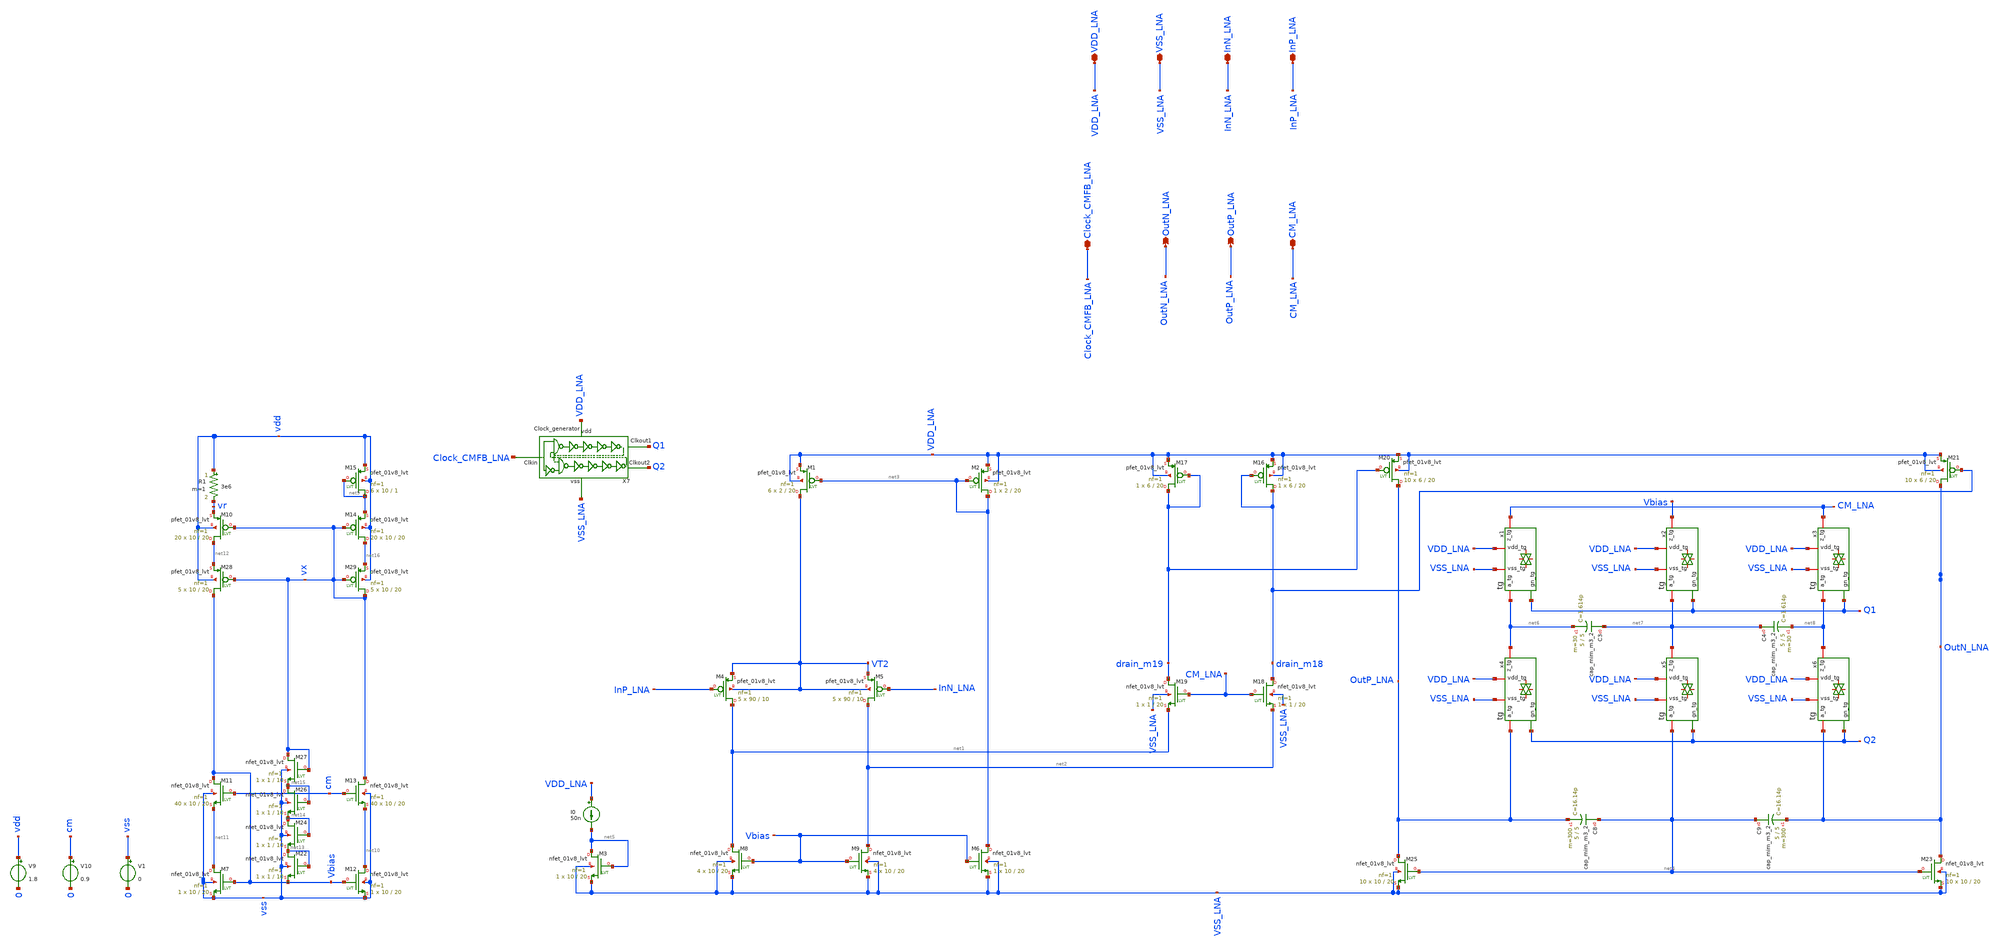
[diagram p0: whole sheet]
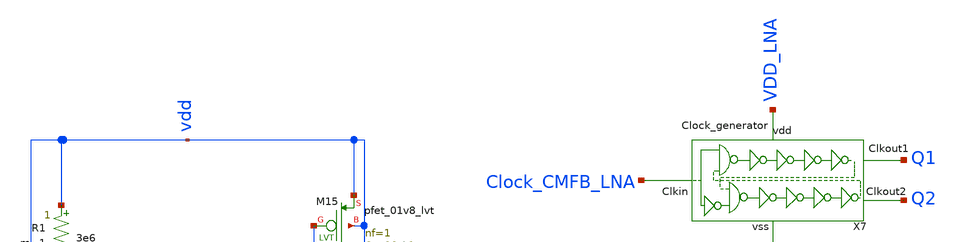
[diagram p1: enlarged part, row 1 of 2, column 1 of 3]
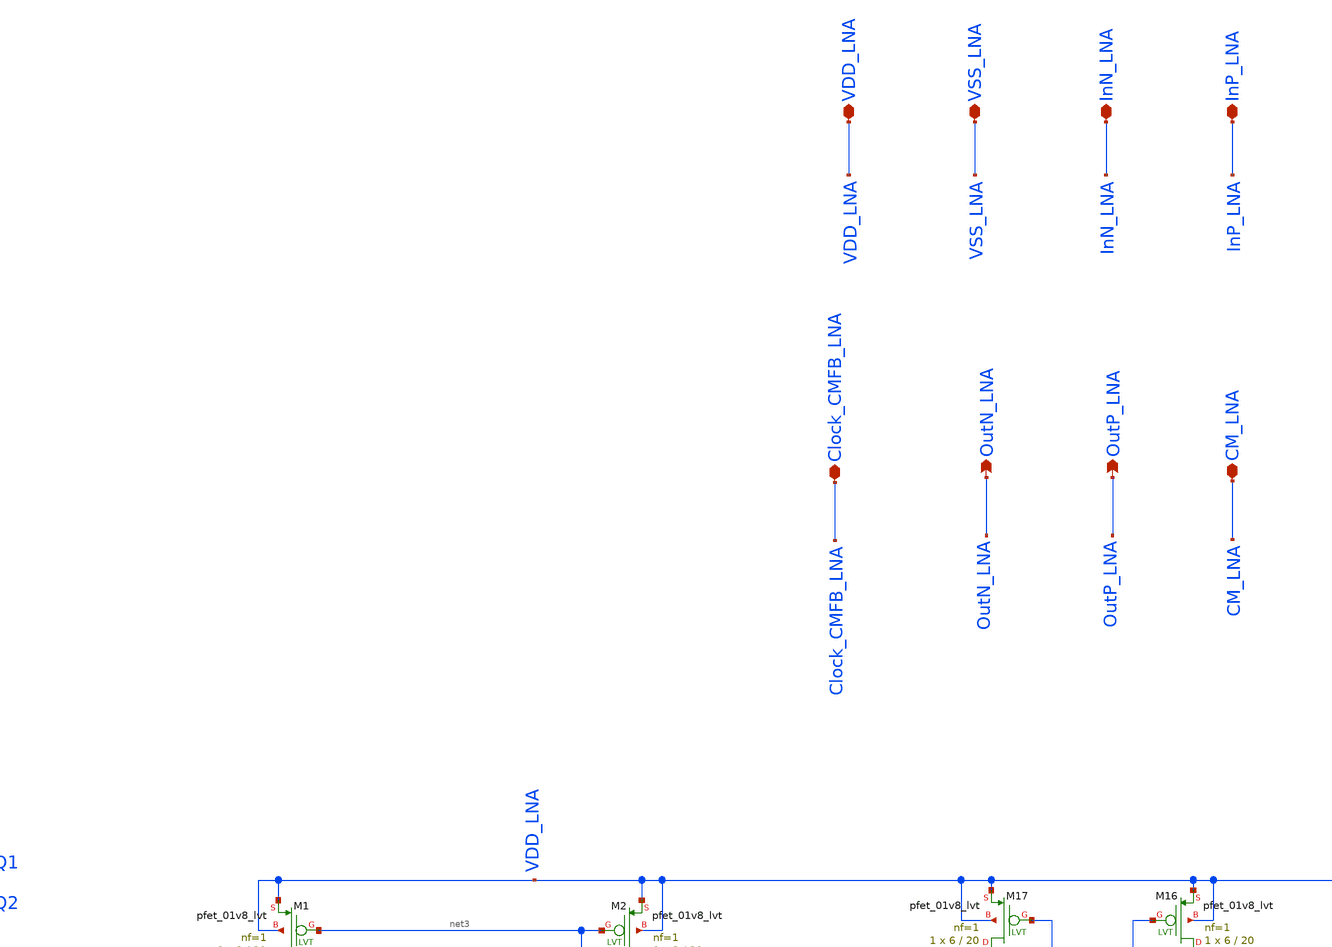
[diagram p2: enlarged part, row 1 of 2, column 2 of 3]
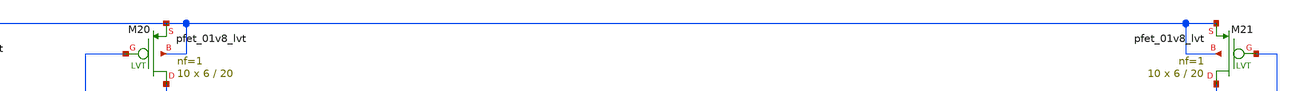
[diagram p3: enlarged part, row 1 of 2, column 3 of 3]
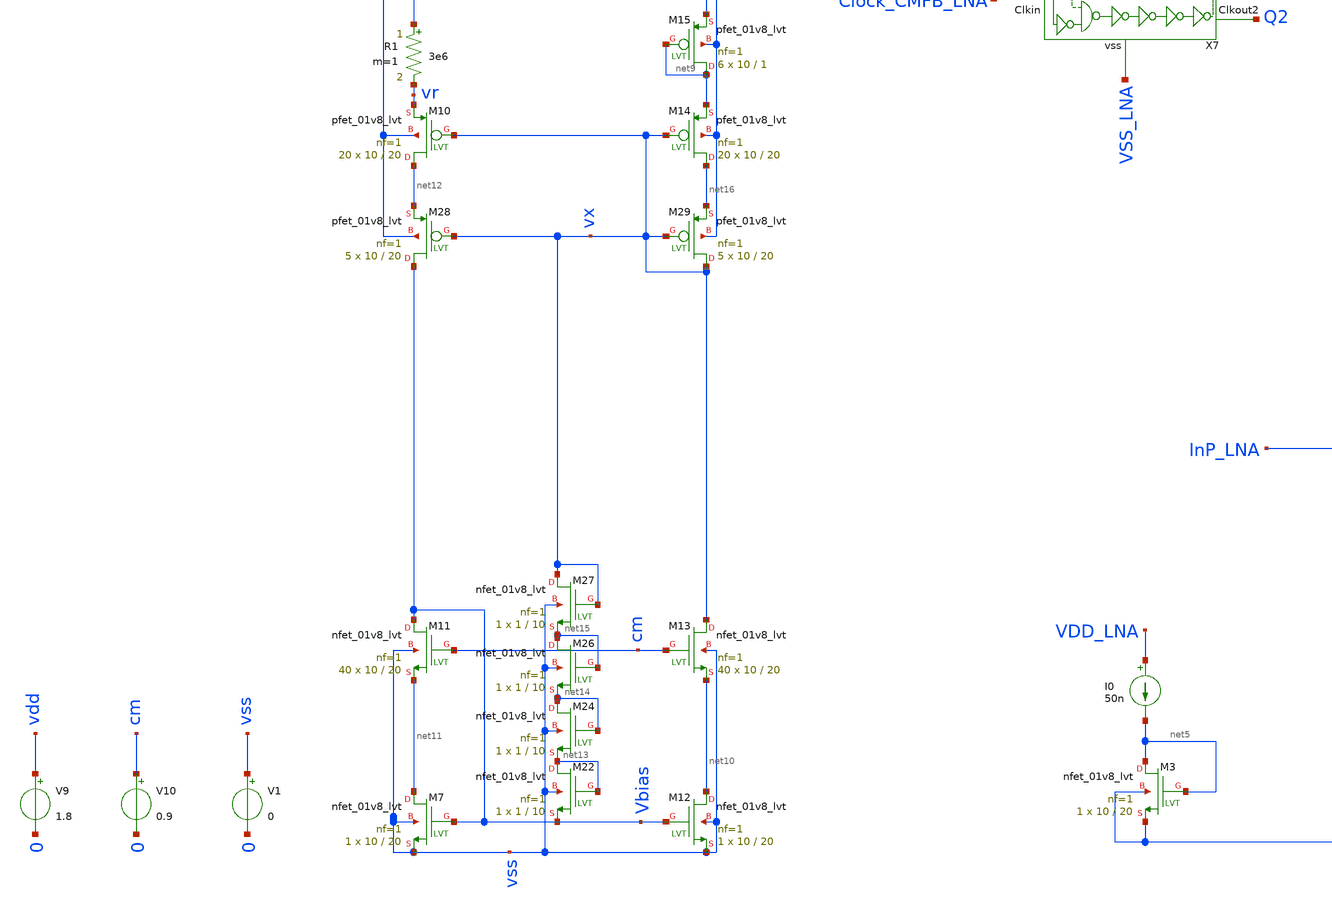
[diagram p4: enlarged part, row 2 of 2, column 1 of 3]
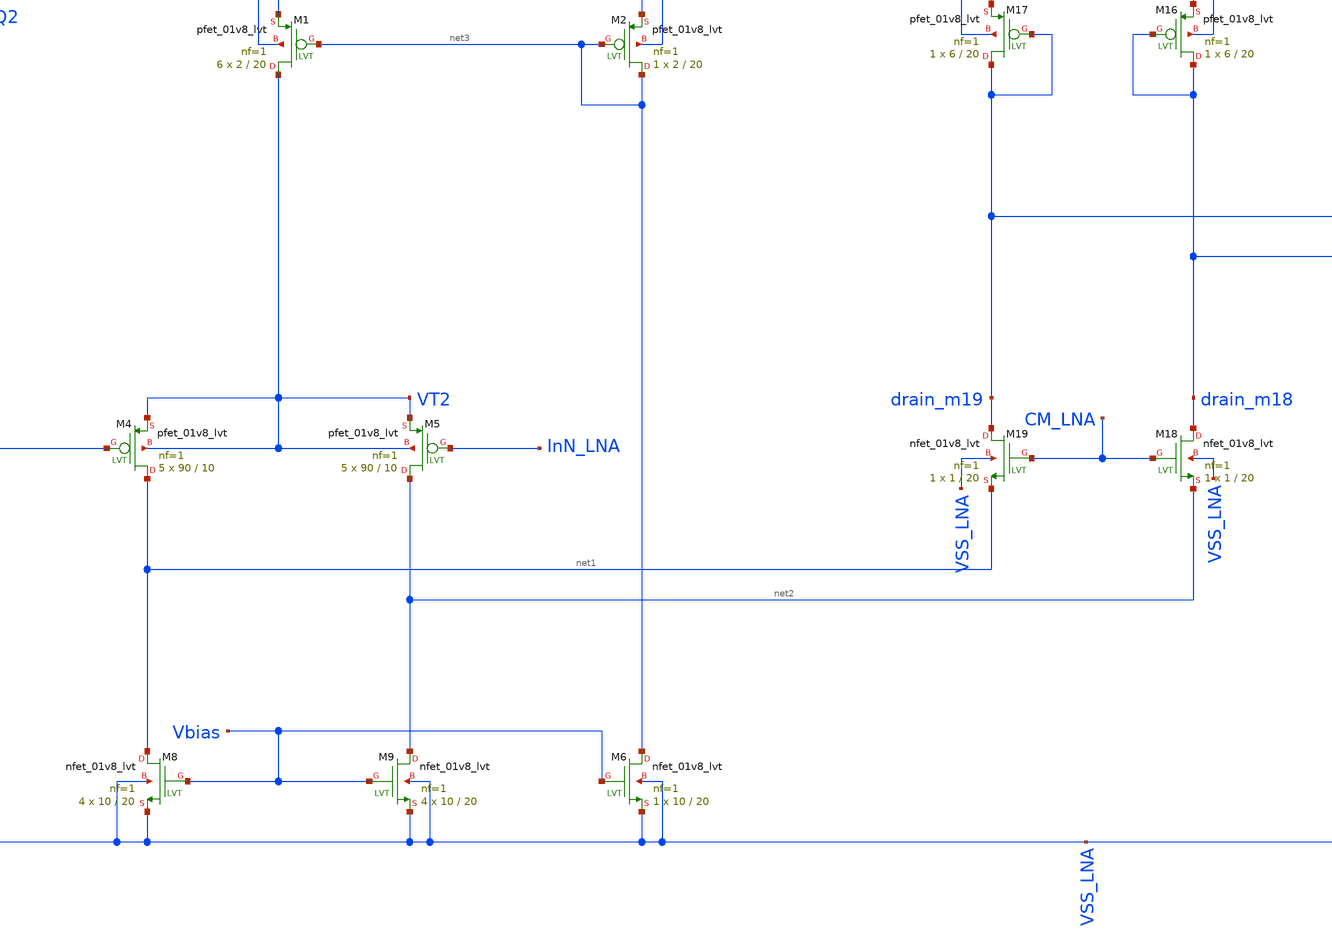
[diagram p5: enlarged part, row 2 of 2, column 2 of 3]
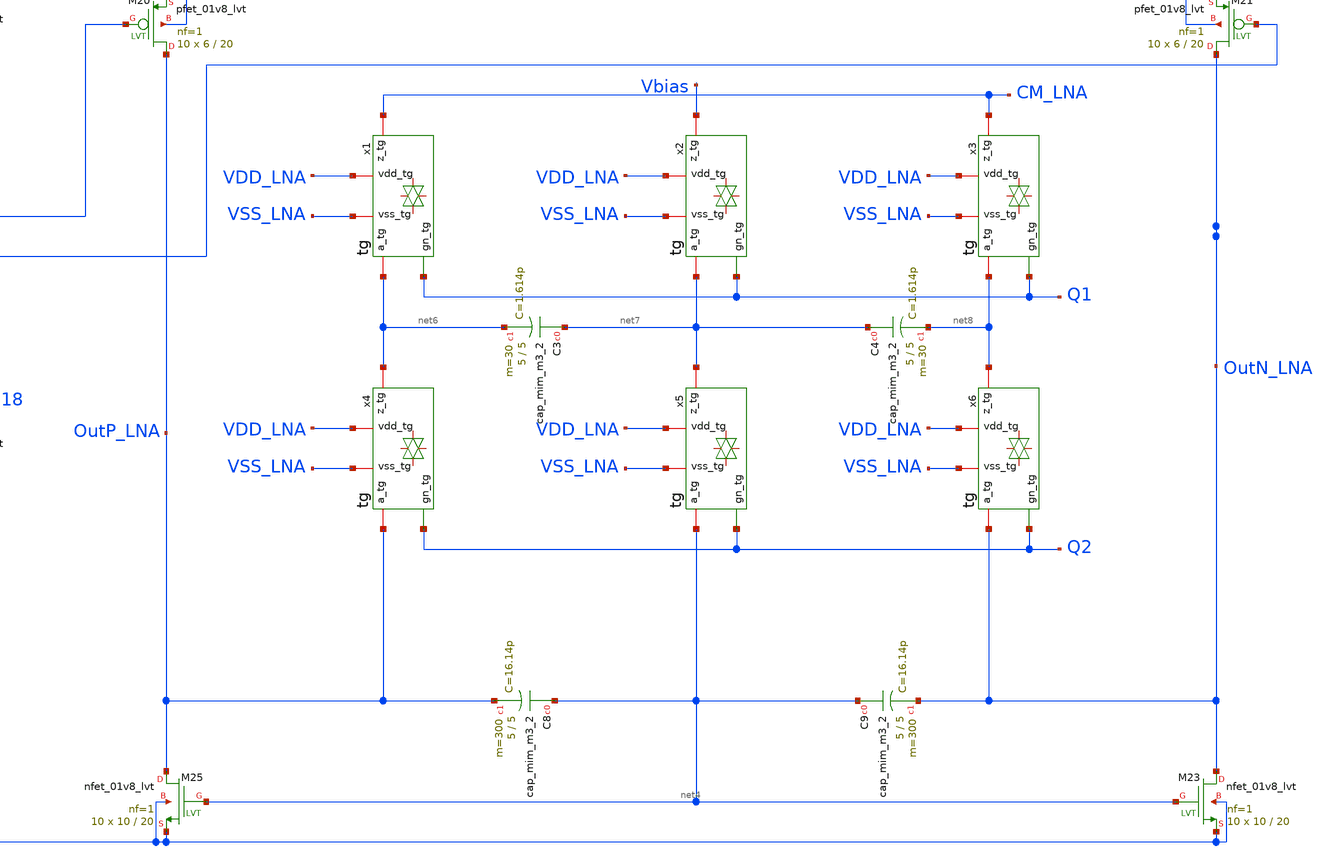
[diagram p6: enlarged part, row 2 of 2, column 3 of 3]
** sch_path: LNA2.sch
**.subckt LNA2 InP_LNA InN_LNA VSS_LNA VDD_LNA CM_LNA OutP_LNA OutN_LNA Clock_CMFB_LNA
*.iopin InP_LNA
*.iopin InN_LNA
*.iopin VSS_LNA
*.iopin VDD_LNA
*.iopin CM_LNA
*.opin OutP_LNA
*.opin OutN_LNA
*.iopin Clock_CMFB_LNA
XM4 net1 InP_LNA VT2 VT2 sky130_fd_pr__pfet_01v8_lvt L=10 W=90 nf=1 ad='int((nf+1)/2) * W/nf * 0.29'
+ as='int((nf+2)/2) * W/nf * 0.29' pd='2*int((nf+1)/2) * (W/nf + 0.29)' ps='2*int((nf+2)/2) * (W/nf + 0.29)'
+ nrd='0.29 / W' nrs='0.29 / W' sa=0 sb=0 sd=0 mult=5 m=5
XM5 net2 InN_LNA VT2 VT2 sky130_fd_pr__pfet_01v8_lvt L=10 W=90 nf=1 ad='int((nf+1)/2) * W/nf * 0.29'
+ as='int((nf+2)/2) * W/nf * 0.29' pd='2*int((nf+1)/2) * (W/nf + 0.29)' ps='2*int((nf+2)/2) * (W/nf + 0.29)'
+ nrd='0.29 / W' nrs='0.29 / W' sa=0 sb=0 sd=0 mult=5 m=5
XM8 net1 Vbias VSS_LNA VSS_LNA sky130_fd_pr__nfet_01v8_lvt L=20 W=10 nf=1 ad='int((nf+1)/2) * W/nf * 0.29'
+ as='int((nf+2)/2) * W/nf * 0.29' pd='2*int((nf+1)/2) * (W/nf + 0.29)' ps='2*int((nf+2)/2) * (W/nf + 0.29)'
+ nrd='0.29 / W' nrs='0.29 / W' sa=0 sb=0 sd=0 mult=4 m=4
XM9 net2 Vbias VSS_LNA VSS_LNA sky130_fd_pr__nfet_01v8_lvt L=20 W=10 nf=1 ad='int((nf+1)/2) * W/nf * 0.29'
+ as='int((nf+2)/2) * W/nf * 0.29' pd='2*int((nf+1)/2) * (W/nf + 0.29)' ps='2*int((nf+2)/2) * (W/nf + 0.29)'
+ nrd='0.29 / W' nrs='0.29 / W' sa=0 sb=0 sd=0 mult=4 m=4
XM16 drain_m18 drain_m18 VDD_LNA VDD_LNA sky130_fd_pr__pfet_01v8_lvt L=20 W=6 nf=1 ad='int((nf+1)/2) * W/nf * 0.29'
+ as='int((nf+2)/2) * W/nf * 0.29' pd='2*int((nf+1)/2) * (W/nf + 0.29)' ps='2*int((nf+2)/2) * (W/nf + 0.29)'
+ nrd='0.29 / W' nrs='0.29 / W' sa=0 sb=0 sd=0 mult=1 m=1
XM17 drain_m19 drain_m19 VDD_LNA VDD_LNA sky130_fd_pr__pfet_01v8_lvt L=20 W=6 nf=1 ad='int((nf+1)/2) * W/nf * 0.29'
+ as='int((nf+2)/2) * W/nf * 0.29' pd='2*int((nf+1)/2) * (W/nf + 0.29)' ps='2*int((nf+2)/2) * (W/nf + 0.29)'
+ nrd='0.29 / W' nrs='0.29 / W' sa=0 sb=0 sd=0 mult=1 m=1
XM18 drain_m18 CM_LNA net2 VSS_LNA sky130_fd_pr__nfet_01v8_lvt L=20 W=1 nf=1 ad='int((nf+1)/2) * W/nf * 0.29'
+ as='int((nf+2)/2) * W/nf * 0.29' pd='2*int((nf+1)/2) * (W/nf + 0.29)' ps='2*int((nf+2)/2) * (W/nf + 0.29)'
+ nrd='0.29 / W' nrs='0.29 / W' sa=0 sb=0 sd=0 mult=1 m=1
XM19 drain_m19 CM_LNA net1 VSS_LNA sky130_fd_pr__nfet_01v8_lvt L=20 W=1 nf=1 ad='int((nf+1)/2) * W/nf * 0.29'
+ as='int((nf+2)/2) * W/nf * 0.29' pd='2*int((nf+1)/2) * (W/nf + 0.29)' ps='2*int((nf+2)/2) * (W/nf + 0.29)'
+ nrd='0.29 / W' nrs='0.29 / W' sa=0 sb=0 sd=0 mult=1 m=1
XM20 OutP_LNA drain_m19 VDD_LNA VDD_LNA sky130_fd_pr__pfet_01v8_lvt L=20 W=6 nf=1 ad='int((nf+1)/2) * W/nf * 0.29'
+ as='int((nf+2)/2) * W/nf * 0.29' pd='2*int((nf+1)/2) * (W/nf + 0.29)' ps='2*int((nf+2)/2) * (W/nf + 0.29)'
+ nrd='0.29 / W' nrs='0.29 / W' sa=0 sb=0 sd=0 mult=10 m=10
XM21 OutN_LNA drain_m18 VDD_LNA VDD_LNA sky130_fd_pr__pfet_01v8_lvt L=20 W=6 nf=1 ad='int((nf+1)/2) * W/nf * 0.29'
+ as='int((nf+2)/2) * W/nf * 0.29' pd='2*int((nf+1)/2) * (W/nf + 0.29)' ps='2*int((nf+2)/2) * (W/nf + 0.29)'
+ nrd='0.29 / W' nrs='0.29 / W' sa=0 sb=0 sd=0 mult=10 m=10
XM23 OutN_LNA net4 VSS_LNA VSS_LNA sky130_fd_pr__nfet_01v8_lvt L=20 W=10 nf=1 ad='int((nf+1)/2) * W/nf * 0.29'
+ as='int((nf+2)/2) * W/nf * 0.29' pd='2*int((nf+1)/2) * (W/nf + 0.29)' ps='2*int((nf+2)/2) * (W/nf + 0.29)'
+ nrd='0.29 / W' nrs='0.29 / W' sa=0 sb=0 sd=0 mult=10 m=10
XM25 OutP_LNA net4 VSS_LNA VSS_LNA sky130_fd_pr__nfet_01v8_lvt L=20 W=10 nf=1 ad='int((nf+1)/2) * W/nf * 0.29'
+ as='int((nf+2)/2) * W/nf * 0.29' pd='2*int((nf+1)/2) * (W/nf + 0.29)' ps='2*int((nf+2)/2) * (W/nf + 0.29)'
+ nrd='0.29 / W' nrs='0.29 / W' sa=0 sb=0 sd=0 mult=10 m=10
XM1 VT2 net3 VDD_LNA VDD_LNA sky130_fd_pr__pfet_01v8_lvt L=20 W=2 nf=1 ad='int((nf+1)/2) * W/nf * 0.29'
+ as='int((nf+2)/2) * W/nf * 0.29' pd='2*int((nf+1)/2) * (W/nf + 0.29)' ps='2*int((nf+2)/2) * (W/nf + 0.29)'
+ nrd='0.29 / W' nrs='0.29 / W' sa=0 sb=0 sd=0 mult=6 m=6
XM2 net3 net3 VDD_LNA VDD_LNA sky130_fd_pr__pfet_01v8_lvt L=20 W=2 nf=1 ad='int((nf+1)/2) * W/nf * 0.29'
+ as='int((nf+2)/2) * W/nf * 0.29' pd='2*int((nf+1)/2) * (W/nf + 0.29)' ps='2*int((nf+2)/2) * (W/nf + 0.29)'
+ nrd='0.29 / W' nrs='0.29 / W' sa=0 sb=0 sd=0 mult=1 m=1
I0 VDD_LNA net5 50n
XM3 net5 net5 VSS_LNA VSS_LNA sky130_fd_pr__nfet_01v8_lvt L=20 W=10 nf=1 ad='int((nf+1)/2) * W/nf * 0.29'
+ as='int((nf+2)/2) * W/nf * 0.29' pd='2*int((nf+1)/2) * (W/nf + 0.29)' ps='2*int((nf+2)/2) * (W/nf + 0.29)'
+ nrd='0.29 / W' nrs='0.29 / W' sa=0 sb=0 sd=0 mult=1 m=1
XM6 net3 Vbias VSS_LNA VSS_LNA sky130_fd_pr__nfet_01v8_lvt L=20 W=10 nf=1 ad='int((nf+1)/2) * W/nf * 0.29'
+ as='int((nf+2)/2) * W/nf * 0.29' pd='2*int((nf+1)/2) * (W/nf + 0.29)' ps='2*int((nf+2)/2) * (W/nf + 0.29)'
+ nrd='0.29 / W' nrs='0.29 / W' sa=0 sb=0 sd=0 mult=1 m=1
XC3 net7 net6 sky130_fd_pr__cap_mim_m3_2 W=5 L=5 MF=30 m=30
XC4 net7 net8 sky130_fd_pr__cap_mim_m3_2 W=5 L=5 MF=30 m=30
XC8 net4 OutP_LNA sky130_fd_pr__cap_mim_m3_2 W=5 L=5 MF=300 m=300
XC9 net4 OutN_LNA sky130_fd_pr__cap_mim_m3_2 W=5 L=5 MF=300 m=300
x1 VDD_LNA net6 CM_LNA VSS_LNA Q1 tg
x2 VDD_LNA net7 Vbias VSS_LNA Q1 tg
x3 VDD_LNA net8 CM_LNA VSS_LNA Q1 tg
x4 VDD_LNA OutP_LNA net6 VSS_LNA Q2 tg
x5 VDD_LNA net4 net7 VSS_LNA Q2 tg
x6 VDD_LNA OutN_LNA net8 VSS_LNA Q2 tg
X7 Clock_CMFB_LNA VSS_LNA Q1 Q2 VDD_LNA Clock_generator
V9 vdd 0 1.8
V10 cm 0 0.9
V1 vss 0 0
XM7 net11 Vbias vss vss sky130_fd_pr__nfet_01v8_lvt L=20 W=10 nf=1 ad='int((nf+1)/2) * W/nf * 0.29' as='int((nf+2)/2) * W/nf * 0.29'
+ pd='2*int((nf+1)/2) * (W/nf + 0.29)' ps='2*int((nf+2)/2) * (W/nf + 0.29)' nrd='0.29 / W' nrs='0.29 / W'
+ sa=0 sb=0 sd=0 mult=1 m=1
XM10 net12 vx vr vdd sky130_fd_pr__pfet_01v8_lvt L=20 W=10 nf=1 ad='int((nf+1)/2) * W/nf * 0.29' as='int((nf+2)/2) * W/nf * 0.29'
+ pd='2*int((nf+1)/2) * (W/nf + 0.29)' ps='2*int((nf+2)/2) * (W/nf + 0.29)' nrd='0.29 / W' nrs='0.29 / W'
+ sa=0 sb=0 sd=0 mult=20 m=20
XM11 Vbias cm net11 vss sky130_fd_pr__nfet_01v8_lvt L=20 W=10 nf=1 ad='int((nf+1)/2) * W/nf * 0.29' as='int((nf+2)/2) * W/nf * 0.29'
+ pd='2*int((nf+1)/2) * (W/nf + 0.29)' ps='2*int((nf+2)/2) * (W/nf + 0.29)' nrd='0.29 / W' nrs='0.29 / W'
+ sa=0 sb=0 sd=0 mult=40 m=40
XM12 net10 Vbias vss vss sky130_fd_pr__nfet_01v8_lvt L=20 W=10 nf=1 ad='int((nf+1)/2) * W/nf * 0.29'
+ as='int((nf+2)/2) * W/nf * 0.29' pd='2*int((nf+1)/2) * (W/nf + 0.29)' ps='2*int((nf+2)/2) * (W/nf + 0.29)'
+ nrd='0.29 / W' nrs='0.29 / W' sa=0 sb=0 sd=0 mult=1 m=1
XM13 vx cm net10 vss sky130_fd_pr__nfet_01v8_lvt L=20 W=10 nf=1 ad='int((nf+1)/2) * W/nf * 0.29' as='int((nf+2)/2) * W/nf * 0.29'
+ pd='2*int((nf+1)/2) * (W/nf + 0.29)' ps='2*int((nf+2)/2) * (W/nf + 0.29)' nrd='0.29 / W' nrs='0.29 / W'
+ sa=0 sb=0 sd=0 mult=40 m=40
XM14 net16 vx net9 vdd sky130_fd_pr__pfet_01v8_lvt L=20 W=10 nf=1 ad='int((nf+1)/2) * W/nf * 0.29' as='int((nf+2)/2) * W/nf * 0.29'
+ pd='2*int((nf+1)/2) * (W/nf + 0.29)' ps='2*int((nf+2)/2) * (W/nf + 0.29)' nrd='0.29 / W' nrs='0.29 / W'
+ sa=0 sb=0 sd=0 mult=20 m=20
XM15 net9 net9 vdd vdd sky130_fd_pr__pfet_01v8_lvt L=1 W=10 nf=1 ad='int((nf+1)/2) * W/nf * 0.29' as='int((nf+2)/2) * W/nf * 0.29'
+ pd='2*int((nf+1)/2) * (W/nf + 0.29)' ps='2*int((nf+2)/2) * (W/nf + 0.29)' nrd='0.29 / W' nrs='0.29 / W'
+ sa=0 sb=0 sd=0 mult=6 m=6
XM22 net13 net13 Vbias vss sky130_fd_pr__nfet_01v8_lvt L=10 W=1 nf=1 ad='int((nf+1)/2) * W/nf * 0.29'
+ as='int((nf+2)/2) * W/nf * 0.29' pd='2*int((nf+1)/2) * (W/nf + 0.29)' ps='2*int((nf+2)/2) * (W/nf + 0.29)'
+ nrd='0.29 / W' nrs='0.29 / W' sa=0 sb=0 sd=0 mult=1 m=1
XM24 net14 net14 net13 vss sky130_fd_pr__nfet_01v8_lvt L=10 W=1 nf=1 ad='int((nf+1)/2) * W/nf * 0.29'
+ as='int((nf+2)/2) * W/nf * 0.29' pd='2*int((nf+1)/2) * (W/nf + 0.29)' ps='2*int((nf+2)/2) * (W/nf + 0.29)'
+ nrd='0.29 / W' nrs='0.29 / W' sa=0 sb=0 sd=0 mult=1 m=1
XM26 net15 net15 net14 vss sky130_fd_pr__nfet_01v8_lvt L=10 W=1 nf=1 ad='int((nf+1)/2) * W/nf * 0.29'
+ as='int((nf+2)/2) * W/nf * 0.29' pd='2*int((nf+1)/2) * (W/nf + 0.29)' ps='2*int((nf+2)/2) * (W/nf + 0.29)'
+ nrd='0.29 / W' nrs='0.29 / W' sa=0 sb=0 sd=0 mult=1 m=1
XM27 vx vx net15 vss sky130_fd_pr__nfet_01v8_lvt L=10 W=1 nf=1 ad='int((nf+1)/2) * W/nf * 0.29' as='int((nf+2)/2) * W/nf * 0.29'
+ pd='2*int((nf+1)/2) * (W/nf + 0.29)' ps='2*int((nf+2)/2) * (W/nf + 0.29)' nrd='0.29 / W' nrs='0.29 / W'
+ sa=0 sb=0 sd=0 mult=1 m=1
XM28 Vbias vx net12 vdd sky130_fd_pr__pfet_01v8_lvt L=20 W=10 nf=1 ad='int((nf+1)/2) * W/nf * 0.29' as='int((nf+2)/2) * W/nf * 0.29'
+ pd='2*int((nf+1)/2) * (W/nf + 0.29)' ps='2*int((nf+2)/2) * (W/nf + 0.29)' nrd='0.29 / W' nrs='0.29 / W'
+ sa=0 sb=0 sd=0 mult=5 m=5
XM29 vx vx net16 vdd sky130_fd_pr__pfet_01v8_lvt L=20 W=10 nf=1 ad='int((nf+1)/2) * W/nf * 0.29' as='int((nf+2)/2) * W/nf * 0.29'
+ pd='2*int((nf+1)/2) * (W/nf + 0.29)' ps='2*int((nf+2)/2) * (W/nf + 0.29)' nrd='0.29 / W' nrs='0.29 / W'
+ sa=0 sb=0 sd=0 mult=5 m=5
R1 vdd vr 3e6 m=1
**.ends

* expanding   symbol:  LNA/tg.sym # of pins=5
** sym_path: tg.sym
** sch_path: tg.sch
.subckt tg vdd_tg a_tg z_tg vss_tg gn_tg
*.iopin a_tg
*.iopin z_tg
*.ipin gn_tg
*.iopin vss_tg
*.iopin vdd_tg
XM1 a_tg gn_tg z_tg vss_tg sky130_fd_pr__nfet_01v8 L=0.2 W=1 nf=1 ad='int((nf+1)/2) * W/nf * 0.29' as='int((nf+2)/2) * W/nf * 0.29'
+ pd='2*int((nf+1)/2) * (W/nf + 0.29)' ps='2*int((nf+2)/2) * (W/nf + 0.29)' nrd='0.29 / W' nrs='0.29 / W'
+ sa=0 sb=0 sd=0 mult=1 m=1
XM2 a_tg net1 z_tg vdd_tg sky130_fd_pr__pfet_01v8 L=0.2 W=2 nf=2 ad='int((nf+1)/2) * W/nf * 0.29' as='int((nf+2)/2) * W/nf * 0.29'
+ pd='2*int((nf+1)/2) * (W/nf + 0.29)' ps='2*int((nf+2)/2) * (W/nf + 0.29)' nrd='0.29 / W' nrs='0.29 / W'
+ sa=0 sb=0 sd=0 mult=1 m=1
x10 gn_tg vss_tg vss_tg vdd_tg vdd_tg net1 sky130_fd_sc_hd__inv_1
.ends


* expanding   symbol:  LNA/Clock_generator.sym # of pins=5
** sym_path: Clock_generator.sym
** sch_path: Clock_generator.sch
.subckt Clock_generator clkin vss clkout1 clkout2 vdd
*.ipin clkin
*.opin clkout1
*.opin clkout2
*.iopin vss
*.iopin vdd
x1 clkin net9 vss vss vdd vdd net1 sky130_fd_sc_hd__nand2_1
x2 net1 vss vss vdd vdd net2 sky130_fd_sc_hd__inv_1
x3 net2 vss vss vdd vdd net3 sky130_fd_sc_hd__inv_1
x4 net3 vss vss vdd vdd clkout1 sky130_fd_sc_hd__inv_1
x5 clkout1 vss vss vdd vdd net5 sky130_fd_sc_hd__inv_1
x6 clkin vss vss vdd vdd net4 sky130_fd_sc_hd__inv_1
x7 net5 net4 vss vss vdd vdd net6 sky130_fd_sc_hd__nand2_1
x19 net6 vss vss vdd vdd net7 sky130_fd_sc_hd__inv_1
x20 net7 vss vss vdd vdd net8 sky130_fd_sc_hd__inv_1
x21 net8 vss vss vdd vdd clkout2 sky130_fd_sc_hd__inv_1
x22 clkout2 vss vss vdd vdd net9 sky130_fd_sc_hd__inv_1
.ends

.end
